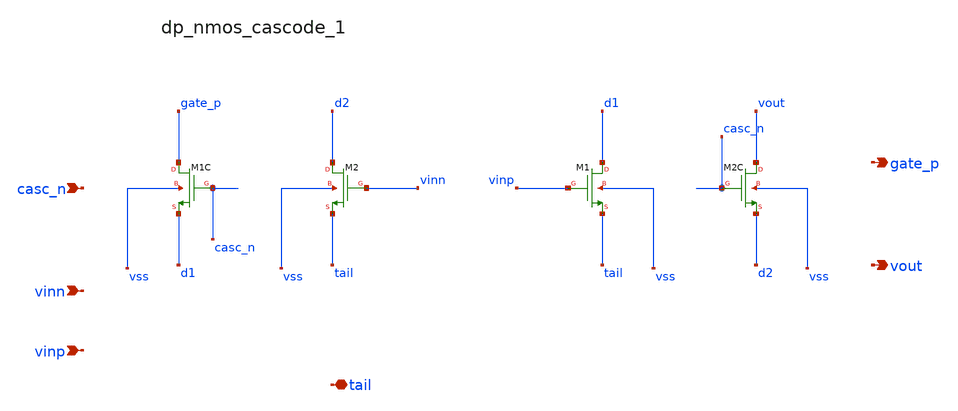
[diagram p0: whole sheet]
** sch_path: analog-db/raw/amp_018_telescopic_cascode/hier/blocks/dp_nmos_cascode_1.sch
**.subckt dp_nmos_cascode_1 casc_n vinn vinp tail gate_p vout
*.ipin casc_n
*.ipin vinn
*.ipin vinp
*.iopin tail
*.opin gate_p
*.opin vout
XM1 d1 vinp tail vss sg13_lv_nmos w=x_dut_xm1_w l=x_dut_xm1_l ng=1 m=x_dut_xm1_m
XM1C gate_p casc_n d1 vss sg13_lv_nmos w=x_dut_xm1c_w l=x_dut_xm1c_l ng=1 m=x_dut_xm1c_m
XM2 d2 vinn tail vss sg13_lv_nmos w=x_dut_xm2_w l=x_dut_xm2_l ng=1 m=x_dut_xm2_m
XM2C vout casc_n d2 vss sg13_lv_nmos w=x_dut_xm2c_w l=x_dut_xm2c_l ng=1 m=x_dut_xm2c_m
**.ends
.end
